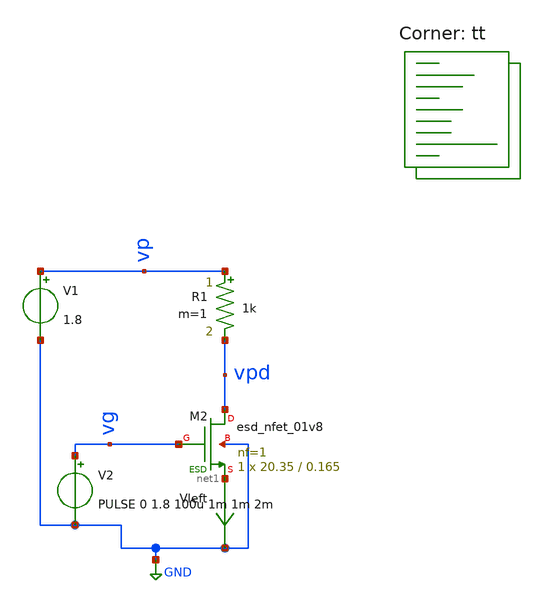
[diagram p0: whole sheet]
** sch_path: Schematics/mos_test.sch
**.subckt mos_test
V1 vp GND 1.8
.save i(v1)
R1 vp vpd 1k m=1
V2 vg GND PULSE 0 1.8 100u 1m 1m 2m
.save i(v2)
XM2 vpd vg net1 GND sky130_fd_pr__esd_nfet_01v8 L=0.165 W=20.35 nf=1 ad='int((nf+1)/2) * W/nf * 0.29'
+ as='int((nf+2)/2) * W/nf * 0.29' pd='2*int((nf+1)/2) * (W/nf + 0.29)' ps='2*int((nf+2)/2) * (W/nf + 0.29)'
+ nrd='0.29 / W' nrs='0.29 / W' sa=0 sb=0 sd=0 mult=1 m=1
Vleft net1 GND 0
.save i(vleft)
**** begin user architecture code
.lib $::SKYWATER_MODELS/sky130.lib.spice tt
**** end user architecture code
**.ends
.GLOBAL GND
**** begin user architecture code

*.options savecurrents
.tran 10u 1.2m
.save all
.control
	run
	write mos_test.raw
.endc


**** end user architecture code
.end
